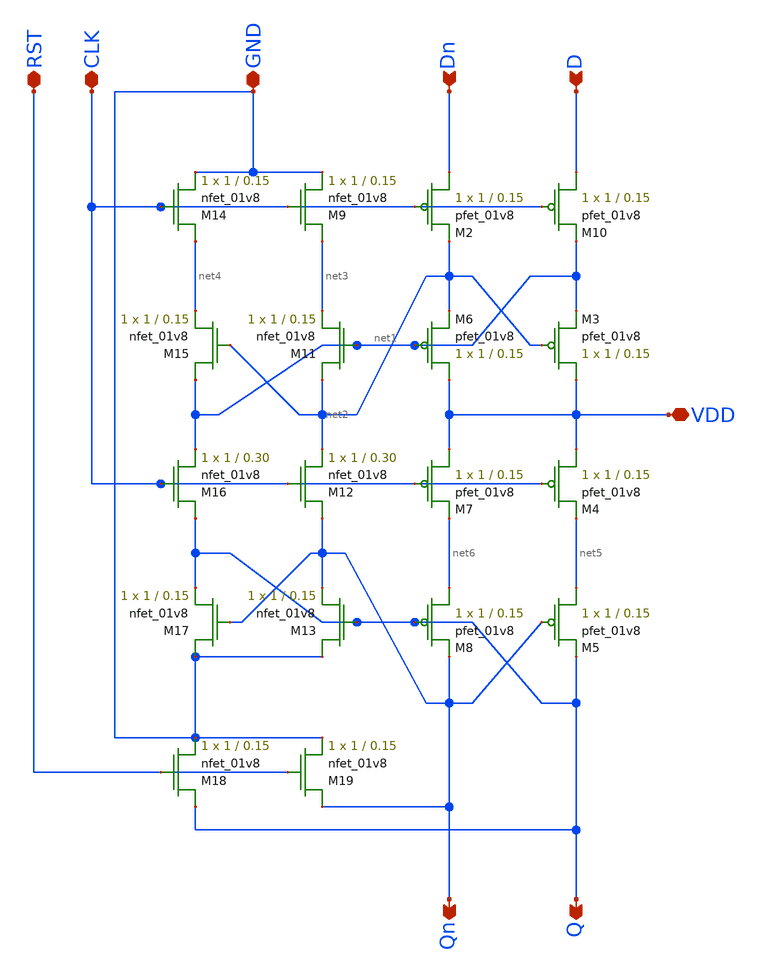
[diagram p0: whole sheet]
** sch_path: shift register/full_shift_register_read.sch
**.subckt full_shift_register_read Q Qn VDD GND D Dn CLK RST
*.opin Q
*.opin Qn
*.iopin VDD
*.iopin GND
*.ipin D
*.ipin Dn
*.iopin CLK
*.iopin RST
XM2 Dn CLK net2 VDD sky130_fd_pr__pfet_01v8 L=0.15 W=1 nf=1 ad='int((nf+1)/2) * W/nf * 0.29' as='int((nf+2)/2) * W/nf * 0.29'
+ pd='2*int((nf+1)/2) * (W/nf + 0.29)' ps='2*int((nf+2)/2) * (W/nf + 0.29)' nrd='0.29 / W' nrs='0.29 / W'
+ sa=0 sb=0 sd=0 mult=1 m=1
XM3 VDD net2 net1 VDD sky130_fd_pr__pfet_01v8 L=0.15 W=1 nf=1 ad='int((nf+1)/2) * W/nf * 0.29' as='int((nf+2)/2) * W/nf * 0.29'
+ pd='2*int((nf+1)/2) * (W/nf + 0.29)' ps='2*int((nf+2)/2) * (W/nf + 0.29)' nrd='0.29 / W' nrs='0.29 / W'
+ sa=0 sb=0 sd=0 mult=1 m=1
XM4 VDD CLK net5 VDD sky130_fd_pr__pfet_01v8 L=0.15 W=1 nf=1 ad='int((nf+1)/2) * W/nf * 0.29' as='int((nf+2)/2) * W/nf * 0.29'
+ pd='2*int((nf+1)/2) * (W/nf + 0.29)' ps='2*int((nf+2)/2) * (W/nf + 0.29)' nrd='0.29 / W' nrs='0.29 / W'
+ sa=0 sb=0 sd=0 mult=1 m=1
XM5 net5 Qn Q VDD sky130_fd_pr__pfet_01v8 L=0.15 W=1 nf=1 ad='int((nf+1)/2) * W/nf * 0.29' as='int((nf+2)/2) * W/nf * 0.29'
+ pd='2*int((nf+1)/2) * (W/nf + 0.29)' ps='2*int((nf+2)/2) * (W/nf + 0.29)' nrd='0.29 / W' nrs='0.29 / W'
+ sa=0 sb=0 sd=0 mult=1 m=1
XM6 VDD net1 net2 VDD sky130_fd_pr__pfet_01v8 L=0.15 W=1 nf=1 ad='int((nf+1)/2) * W/nf * 0.29' as='int((nf+2)/2) * W/nf * 0.29'
+ pd='2*int((nf+1)/2) * (W/nf + 0.29)' ps='2*int((nf+2)/2) * (W/nf + 0.29)' nrd='0.29 / W' nrs='0.29 / W'
+ sa=0 sb=0 sd=0 mult=1 m=1
XM7 VDD CLK net6 VDD sky130_fd_pr__pfet_01v8 L=0.15 W=1 nf=1 ad='int((nf+1)/2) * W/nf * 0.29' as='int((nf+2)/2) * W/nf * 0.29'
+ pd='2*int((nf+1)/2) * (W/nf + 0.29)' ps='2*int((nf+2)/2) * (W/nf + 0.29)' nrd='0.29 / W' nrs='0.29 / W'
+ sa=0 sb=0 sd=0 mult=1 m=1
XM8 net6 Q Qn VDD sky130_fd_pr__pfet_01v8 L=0.15 W=1 nf=1 ad='int((nf+1)/2) * W/nf * 0.29' as='int((nf+2)/2) * W/nf * 0.29'
+ pd='2*int((nf+1)/2) * (W/nf + 0.29)' ps='2*int((nf+2)/2) * (W/nf + 0.29)' nrd='0.29 / W' nrs='0.29 / W'
+ sa=0 sb=0 sd=0 mult=1 m=1
XM9 net3 CLK GND GND sky130_fd_pr__nfet_01v8 L=0.15 W=1 nf=1 ad='int((nf+1)/2) * W/nf * 0.29' as='int((nf+2)/2) * W/nf * 0.29'
+ pd='2*int((nf+1)/2) * (W/nf + 0.29)' ps='2*int((nf+2)/2) * (W/nf + 0.29)' nrd='0.29 / W' nrs='0.29 / W'
+ sa=0 sb=0 sd=0 mult=1 m=1
XM10 D CLK net1 VDD sky130_fd_pr__pfet_01v8 L=0.15 W=1 nf=1 ad='int((nf+1)/2) * W/nf * 0.29' as='int((nf+2)/2) * W/nf * 0.29'
+ pd='2*int((nf+1)/2) * (W/nf + 0.29)' ps='2*int((nf+2)/2) * (W/nf + 0.29)' nrd='0.29 / W' nrs='0.29 / W'
+ sa=0 sb=0 sd=0 mult=1 m=1
XM11 net2 net1 net3 GND sky130_fd_pr__nfet_01v8 L=0.15 W=1 nf=1 ad='int((nf+1)/2) * W/nf * 0.29' as='int((nf+2)/2) * W/nf * 0.29'
+ pd='2*int((nf+1)/2) * (W/nf + 0.29)' ps='2*int((nf+2)/2) * (W/nf + 0.29)' nrd='0.29 / W' nrs='0.29 / W'
+ sa=0 sb=0 sd=0 mult=1 m=1
XM12 Qn CLK net2 GND sky130_fd_pr__nfet_01v8 L=0.30 W=1 nf=1 ad='int((nf+1)/2) * W/nf * 0.29' as='int((nf+2)/2) * W/nf * 0.29'
+ pd='2*int((nf+1)/2) * (W/nf + 0.29)' ps='2*int((nf+2)/2) * (W/nf + 0.29)' nrd='0.29 / W' nrs='0.29 / W'
+ sa=0 sb=0 sd=0 mult=1 m=1
XM13 GND Q Qn GND sky130_fd_pr__nfet_01v8 L=0.15 W=1 nf=1 ad='int((nf+1)/2) * W/nf * 0.29' as='int((nf+2)/2) * W/nf * 0.29'
+ pd='2*int((nf+1)/2) * (W/nf + 0.29)' ps='2*int((nf+2)/2) * (W/nf + 0.29)' nrd='0.29 / W' nrs='0.29 / W'
+ sa=0 sb=0 sd=0 mult=1 m=1
XM14 net4 CLK GND GND sky130_fd_pr__nfet_01v8 L=0.15 W=1 nf=1 ad='int((nf+1)/2) * W/nf * 0.29' as='int((nf+2)/2) * W/nf * 0.29'
+ pd='2*int((nf+1)/2) * (W/nf + 0.29)' ps='2*int((nf+2)/2) * (W/nf + 0.29)' nrd='0.29 / W' nrs='0.29 / W'
+ sa=0 sb=0 sd=0 mult=1 m=1
XM15 net1 net2 net4 GND sky130_fd_pr__nfet_01v8 L=0.15 W=1 nf=1 ad='int((nf+1)/2) * W/nf * 0.29' as='int((nf+2)/2) * W/nf * 0.29'
+ pd='2*int((nf+1)/2) * (W/nf + 0.29)' ps='2*int((nf+2)/2) * (W/nf + 0.29)' nrd='0.29 / W' nrs='0.29 / W'
+ sa=0 sb=0 sd=0 mult=1 m=1
XM16 Q CLK net1 GND sky130_fd_pr__nfet_01v8 L=0.30 W=1 nf=1 ad='int((nf+1)/2) * W/nf * 0.29' as='int((nf+2)/2) * W/nf * 0.29'
+ pd='2*int((nf+1)/2) * (W/nf + 0.29)' ps='2*int((nf+2)/2) * (W/nf + 0.29)' nrd='0.29 / W' nrs='0.29 / W'
+ sa=0 sb=0 sd=0 mult=1 m=1
XM17 GND Qn Q GND sky130_fd_pr__nfet_01v8 L=0.15 W=1 nf=1 ad='int((nf+1)/2) * W/nf * 0.29' as='int((nf+2)/2) * W/nf * 0.29'
+ pd='2*int((nf+1)/2) * (W/nf + 0.29)' ps='2*int((nf+2)/2) * (W/nf + 0.29)' nrd='0.29 / W' nrs='0.29 / W'
+ sa=0 sb=0 sd=0 mult=1 m=1
XM18 Q RST GND GND sky130_fd_pr__nfet_01v8 L=0.15 W=1 nf=1 ad='int((nf+1)/2) * W/nf * 0.29' as='int((nf+2)/2) * W/nf * 0.29'
+ pd='2*int((nf+1)/2) * (W/nf + 0.29)' ps='2*int((nf+2)/2) * (W/nf + 0.29)' nrd='0.29 / W' nrs='0.29 / W'
+ sa=0 sb=0 sd=0 mult=1 m=1
XM19 Qn RST GND GND sky130_fd_pr__nfet_01v8 L=0.15 W=1 nf=1 ad='int((nf+1)/2) * W/nf * 0.29' as='int((nf+2)/2) * W/nf * 0.29'
+ pd='2*int((nf+1)/2) * (W/nf + 0.29)' ps='2*int((nf+2)/2) * (W/nf + 0.29)' nrd='0.29 / W' nrs='0.29 / W'
+ sa=0 sb=0 sd=0 mult=1 m=1
**.ends
.end
